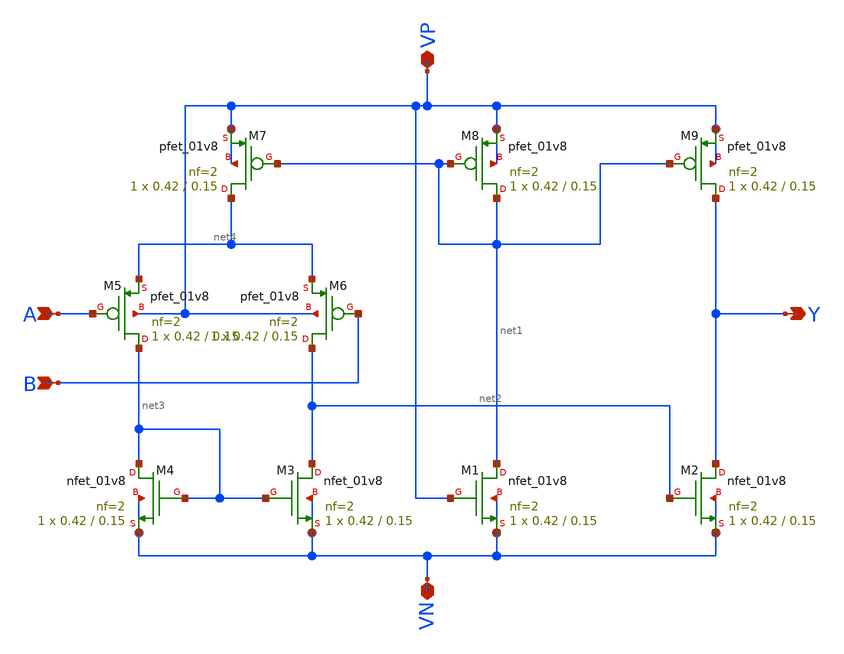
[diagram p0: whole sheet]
** sch_path: week 4/sim/1/opamp.sch
**.subckt opamp Y A B VN VP
*.opin Y
*.ipin A
*.ipin B
*.iopin VN
*.iopin VP
XM1 net1 VP VN VN sky130_fd_pr__nfet_01v8 L=0.15 W=0.42 nf=2 ad='int((nf+1)/2) * W/nf * 0.29' as='int((nf+2)/2) * W/nf * 0.29'
+ pd='2*int((nf+1)/2) * (W/nf + 0.29)' ps='2*int((nf+2)/2) * (W/nf + 0.29)' nrd='0.29 / W' nrs='0.29 / W'
+ sa=0 sb=0 sd=0 mult=1 m=1
XM2 Y net2 VN VN sky130_fd_pr__nfet_01v8 L=0.15 W=0.42 nf=2 ad='int((nf+1)/2) * W/nf * 0.29' as='int((nf+2)/2) * W/nf * 0.29'
+ pd='2*int((nf+1)/2) * (W/nf + 0.29)' ps='2*int((nf+2)/2) * (W/nf + 0.29)' nrd='0.29 / W' nrs='0.29 / W'
+ sa=0 sb=0 sd=0 mult=1 m=1
XM3 net2 net3 VN VN sky130_fd_pr__nfet_01v8 L=0.15 W=0.42 nf=2 ad='int((nf+1)/2) * W/nf * 0.29' as='int((nf+2)/2) * W/nf * 0.29'
+ pd='2*int((nf+1)/2) * (W/nf + 0.29)' ps='2*int((nf+2)/2) * (W/nf + 0.29)' nrd='0.29 / W' nrs='0.29 / W'
+ sa=0 sb=0 sd=0 mult=1 m=1
XM4 net3 net3 VN VN sky130_fd_pr__nfet_01v8 L=0.15 W=0.42 nf=2 ad='int((nf+1)/2) * W/nf * 0.29' as='int((nf+2)/2) * W/nf * 0.29'
+ pd='2*int((nf+1)/2) * (W/nf + 0.29)' ps='2*int((nf+2)/2) * (W/nf + 0.29)' nrd='0.29 / W' nrs='0.29 / W'
+ sa=0 sb=0 sd=0 mult=1 m=1
XM6 net2 B net4 VP sky130_fd_pr__pfet_01v8 L=0.15 W=0.42 nf=2 ad='int((nf+1)/2) * W/nf * 0.29' as='int((nf+2)/2) * W/nf * 0.29'
+ pd='2*int((nf+1)/2) * (W/nf + 0.29)' ps='2*int((nf+2)/2) * (W/nf + 0.29)' nrd='0.29 / W' nrs='0.29 / W'
+ sa=0 sb=0 sd=0 mult=1 m=1
XM5 net3 A net4 VP sky130_fd_pr__pfet_01v8 L=0.15 W=0.42 nf=2 ad='int((nf+1)/2) * W/nf * 0.29' as='int((nf+2)/2) * W/nf * 0.29'
+ pd='2*int((nf+1)/2) * (W/nf + 0.29)' ps='2*int((nf+2)/2) * (W/nf + 0.29)' nrd='0.29 / W' nrs='0.29 / W'
+ sa=0 sb=0 sd=0 mult=1 m=1
XM7 net4 net1 VP VP sky130_fd_pr__pfet_01v8 L=0.15 W=0.42 nf=2 ad='int((nf+1)/2) * W/nf * 0.29' as='int((nf+2)/2) * W/nf * 0.29'
+ pd='2*int((nf+1)/2) * (W/nf + 0.29)' ps='2*int((nf+2)/2) * (W/nf + 0.29)' nrd='0.29 / W' nrs='0.29 / W'
+ sa=0 sb=0 sd=0 mult=1 m=1
XM8 net1 net1 VP VP sky130_fd_pr__pfet_01v8 L=0.15 W=0.42 nf=2 ad='int((nf+1)/2) * W/nf * 0.29' as='int((nf+2)/2) * W/nf * 0.29'
+ pd='2*int((nf+1)/2) * (W/nf + 0.29)' ps='2*int((nf+2)/2) * (W/nf + 0.29)' nrd='0.29 / W' nrs='0.29 / W'
+ sa=0 sb=0 sd=0 mult=1 m=1
XM9 Y net1 VP VP sky130_fd_pr__pfet_01v8 L=0.15 W=0.42 nf=2 ad='int((nf+1)/2) * W/nf * 0.29' as='int((nf+2)/2) * W/nf * 0.29'
+ pd='2*int((nf+1)/2) * (W/nf + 0.29)' ps='2*int((nf+2)/2) * (W/nf + 0.29)' nrd='0.29 / W' nrs='0.29 / W'
+ sa=0 sb=0 sd=0 mult=1 m=1
**.ends
.end
